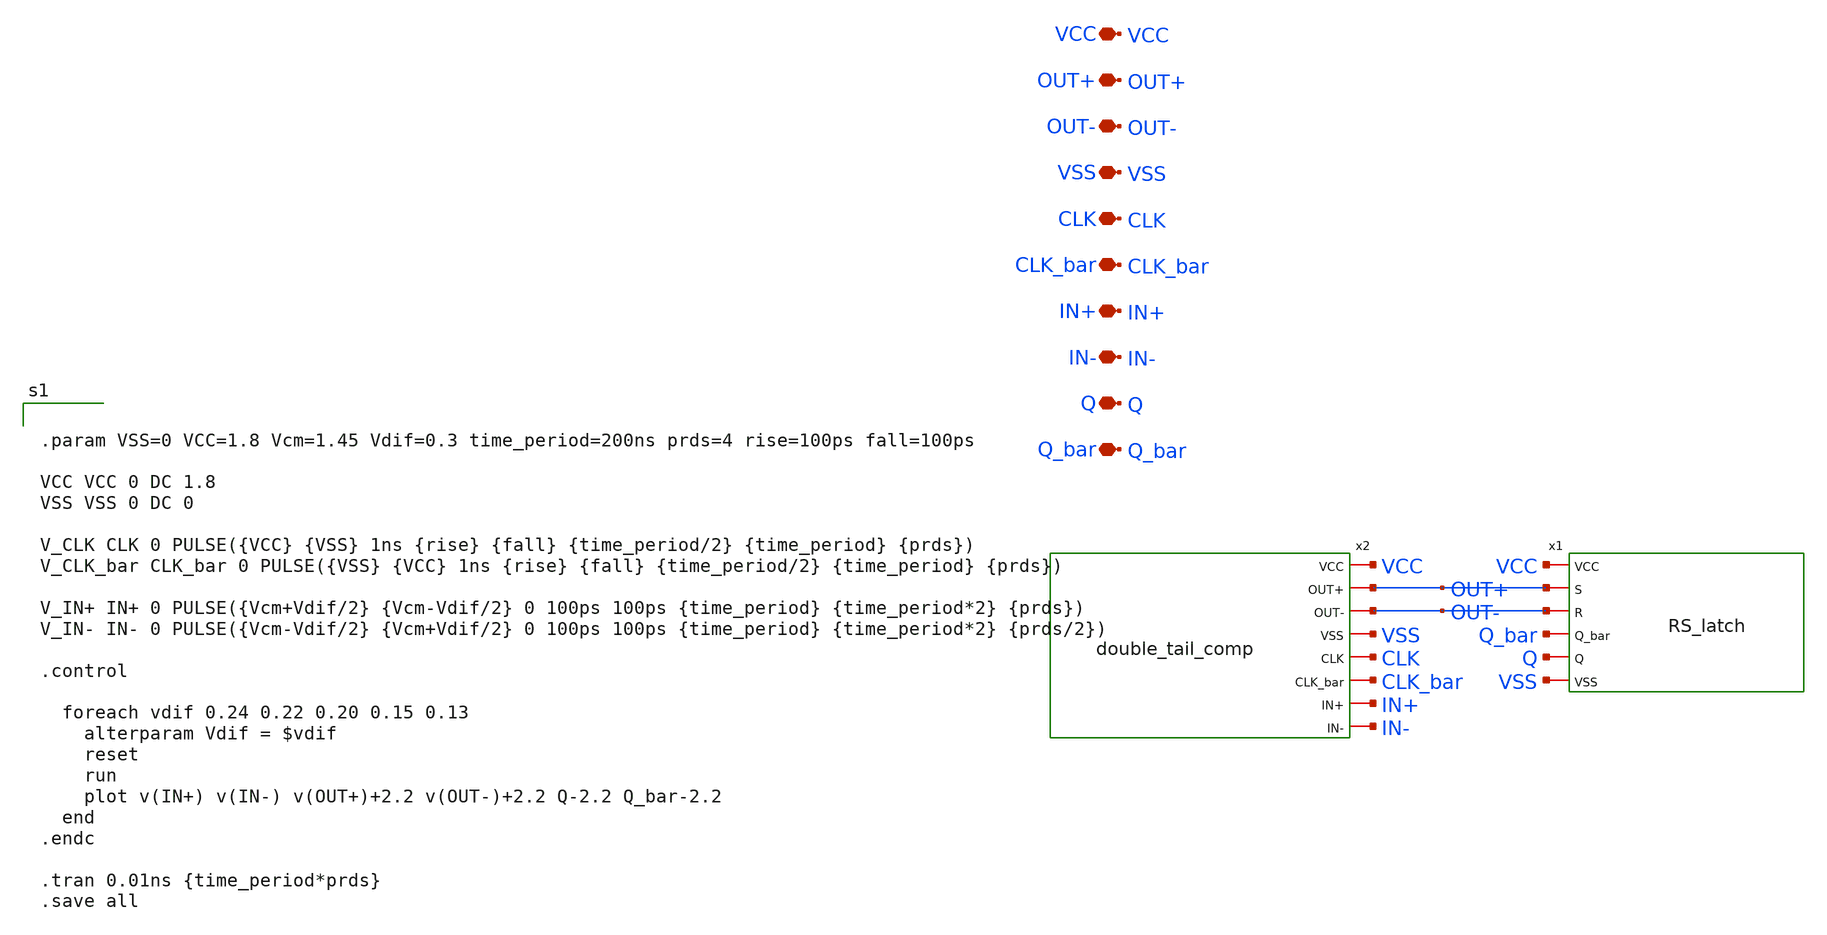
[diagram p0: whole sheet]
** sch_path: voltage_comp/dt-comp_rs_test.sch
**.subckt dt-comp_rs_test OUT- VSS VCC OUT+ IN+ IN- CLK CLK_bar Q Q_bar
*.iopin OUT-
*.iopin VSS
*.iopin VCC
*.iopin OUT+
*.iopin IN+
*.iopin IN-
*.iopin CLK
*.iopin CLK_bar
*.iopin Q
*.iopin Q_bar
x1 VCC OUT- OUT+ Q_bar Q VSS RS_latch
x2 VCC OUT+ OUT- VSS CLK CLK_bar IN+ IN- double_tail_comp
**** begin user architecture code


.param VSS=0 VCC=1.8 Vcm=1.45 Vdif=0.3 time_period=200ns prds=4 rise=100ps fall=100ps

VCC VCC 0 DC 1.8
VSS VSS 0 DC 0

V_CLK CLK 0 PULSE({VCC} {VSS} 1ns {rise} {fall} {time_period/2} {time_period} {prds})
V_CLK_bar CLK_bar 0 PULSE({VSS} {VCC} 1ns {rise} {fall} {time_period/2} {time_period} {prds})

V_IN+ IN+ 0 PULSE({Vcm+Vdif/2} {Vcm-Vdif/2} 0 100ps 100ps {time_period} {time_period*2} {prds})
V_IN- IN- 0 PULSE({Vcm-Vdif/2} {Vcm+Vdif/2} 0 100ps 100ps {time_period} {time_period*2} {prds/2})

.control

  foreach vdif 0.24 0.22 0.20 0.15 0.13
    alterparam Vdif = $vdif
    reset
    run
    plot v(IN+) v(IN-) v(OUT+)+2.2 v(OUT-)+2.2 Q-2.2 Q_bar-2.2
  end
.endc

.tran 0.01ns {time_period*prds}
.save all



** opencircuitdesign pdks install
.lib $::SKYWATER_MODELS/sky130.lib.spice tt

**** end user architecture code
**.ends
.end
